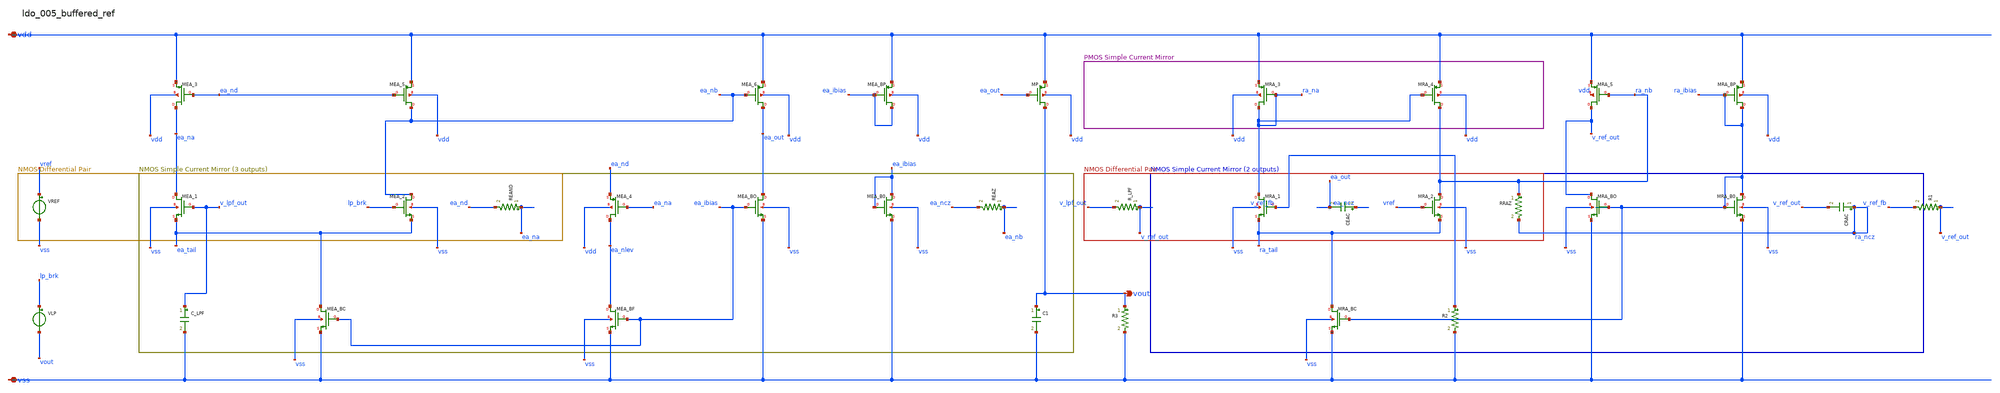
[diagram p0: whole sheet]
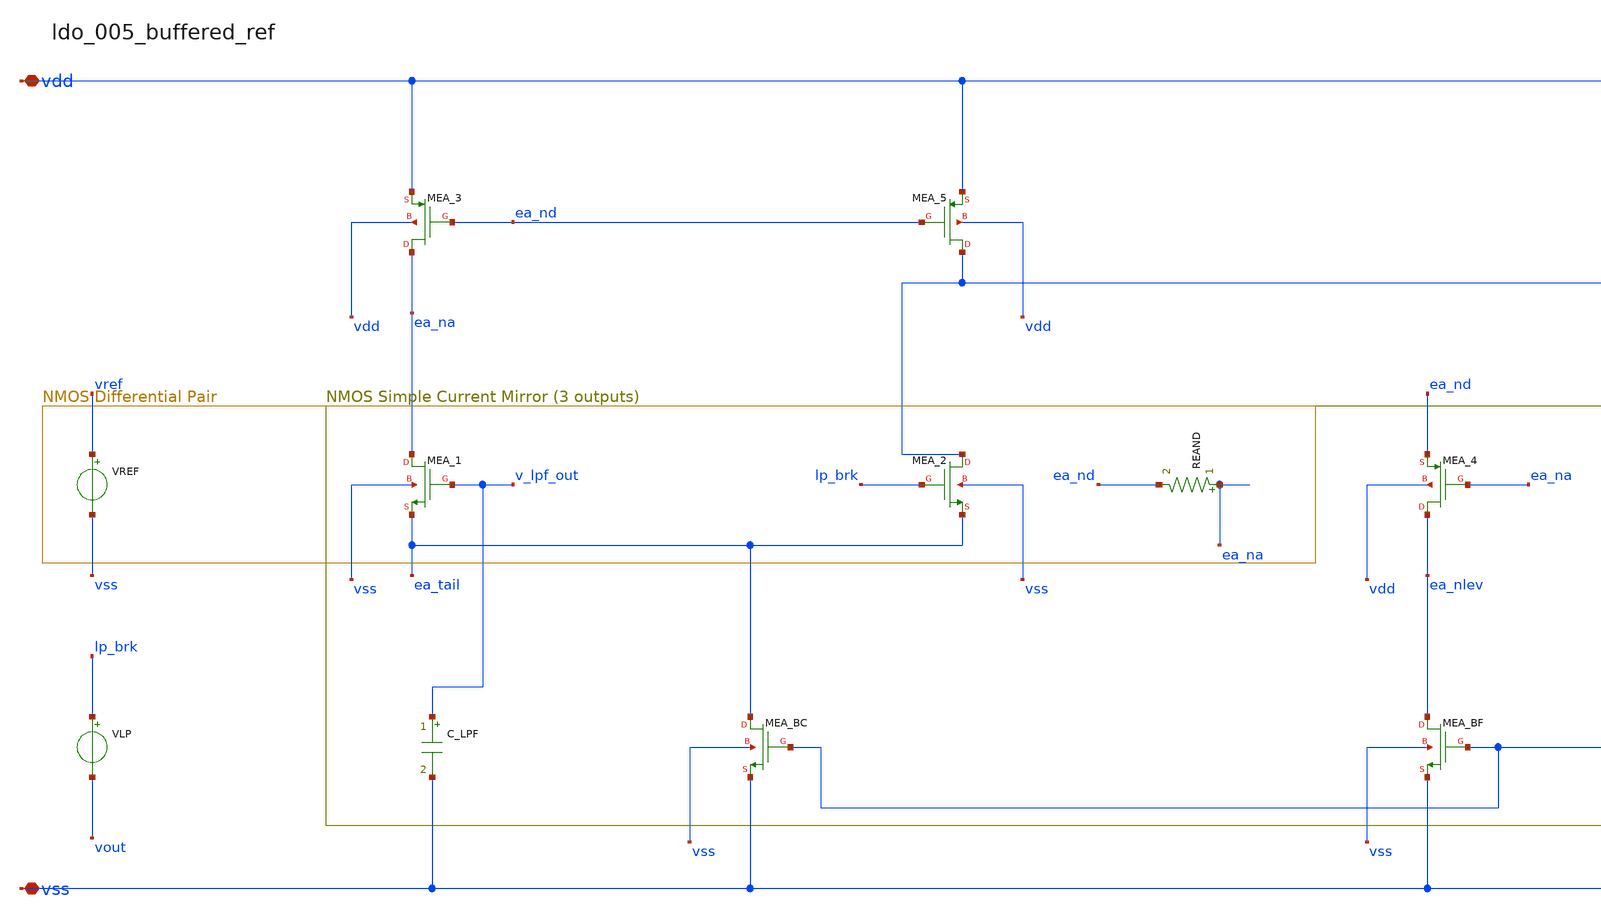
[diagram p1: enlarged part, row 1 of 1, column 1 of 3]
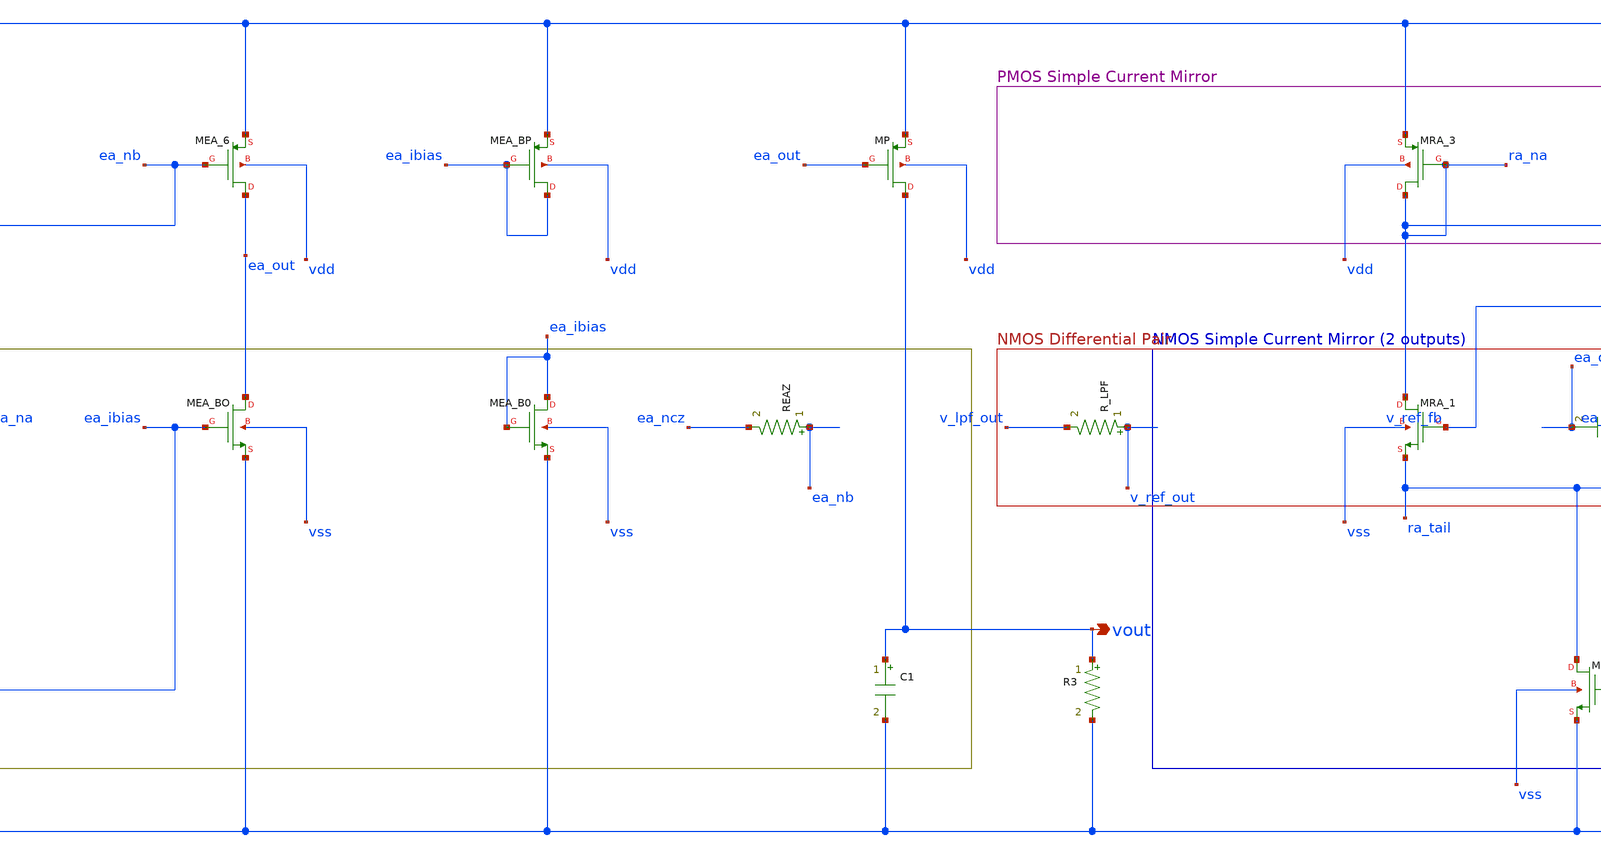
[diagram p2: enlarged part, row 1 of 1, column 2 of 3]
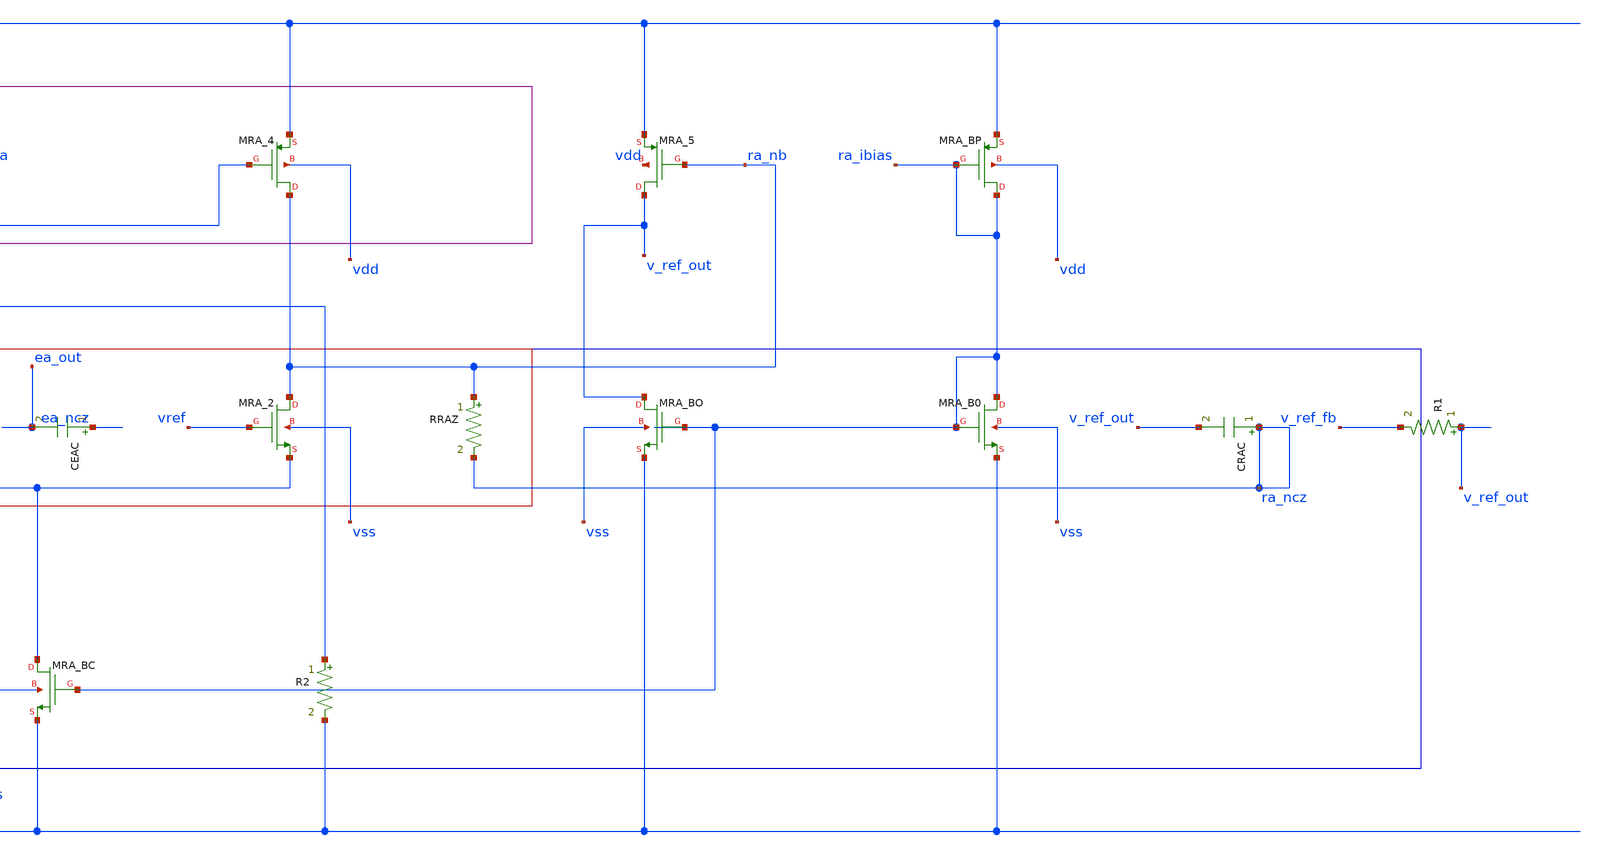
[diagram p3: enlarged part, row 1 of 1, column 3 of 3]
** sch_path: analog-db/raw/ldo_005_buffered_ref/ldo_005_buffered_ref_annotated.sch
**.subckt ldo_005_buffered_ref_annotated vdd vss vout
*.iopin vdd
*.iopin vss
*.opin vout
C1 vout vss 'c_out_int' m=1
CEAC ea_ncz ea_out 'c_ea_comp' m=1
CRAC ra_ncz v_ref_out 'c_ra_comp' m=1
C_LPF v_lpf_out vss 'c_lpf' m=1
R1 v_ref_out v_ref_fb 'r_ref_top' m=1
R2 v_ref_fb vss 'r_ref_bot' m=1
R3 vout vss 'r_bleed' m=1
REAND ea_na ea_nd 'r_ea_nd' m=1
REAZ ea_nb ea_ncz 'r_ea_z' m=1
RRAZ ra_nb ra_ncz 'r_ra_z' m=1
R_LPF v_ref_out v_lpf_out 'r_lpf' m=1
VLP lp_brk vout dc 0
VREF vref vss dc {vref_val}
XMEA_1 ea_na v_lpf_out ea_tail vss sg13_hv_nmos w=x_dut_xmea_1_w l=x_dut_xmea_1_l ng=1 m=1
XMEA_2 ea_nb lp_brk ea_tail vss sg13_hv_nmos w=x_dut_xmea_2_w l=x_dut_xmea_2_l ng=1 m=1
XMEA_3 ea_na ea_nd vdd vdd sg13_hv_pmos w=x_dut_xmea_3_w l=x_dut_xmea_3_l ng=1 m=1
XMEA_4 ea_nlev ea_na ea_nd vdd sg13_hv_pmos w=x_dut_xmea_4_w l=x_dut_xmea_4_l ng=1 m=1
XMEA_5 ea_nb ea_nd vdd vdd sg13_hv_pmos w=x_dut_xmea_5_w l=x_dut_xmea_5_l ng=1 m=1
XMEA_6 ea_out ea_nb vdd vdd sg13_hv_pmos w=x_dut_xmea_6_w l=x_dut_xmea_6_l ng=1 m=1
XMEA_B0 ea_ibias ea_ibias vss vss sg13_hv_nmos w=x_dut_xmea_b0_w l=x_dut_xmea_b0_l ng=1 m=1
XMEA_BC ea_tail ea_ibias vss vss sg13_hv_nmos w=x_dut_xmea_bc_w l=x_dut_xmea_bc_l ng=1 m=1
XMEA_BF ea_nlev ea_ibias vss vss sg13_hv_nmos w=x_dut_xmea_bf_w l=x_dut_xmea_bf_l ng=1 m=1
XMEA_BO ea_out ea_ibias vss vss sg13_hv_nmos w=x_dut_xmea_bo_w l=x_dut_xmea_bo_l ng=1 m=1
XMEA_BP ea_ibias ea_ibias vdd vdd sg13_hv_pmos w=x_dut_xmea_bp_w l=x_dut_xmea_bp_l ng=1 m=1
XMP vout ea_out vdd vdd sg13_hv_pmos w=x_dut_xmp_w l=x_dut_xmp_l ng=1 m=x_dut_xmp_m
XMRA_1 ra_na v_ref_fb ra_tail vss sg13_hv_nmos w=x_dut_xmra_1_w l=x_dut_xmra_1_l ng=1 m=1
XMRA_2 ra_nb vref ra_tail vss sg13_hv_nmos w=x_dut_xmra_2_w l=x_dut_xmra_2_l ng=1 m=1
XMRA_3 ra_na ra_na vdd vdd sg13_hv_pmos w=x_dut_xmra_3_w l=x_dut_xmra_3_l ng=1 m=1
XMRA_4 ra_nb ra_na vdd vdd sg13_hv_pmos w=x_dut_xmra_4_w l=x_dut_xmra_4_l ng=1 m=1
XMRA_5 v_ref_out ra_nb vdd vdd sg13_hv_pmos w=x_dut_xmra_5_w l=x_dut_xmra_5_l ng=1 m=1
XMRA_B0 ra_ibias ra_ibias vss vss sg13_hv_nmos w=x_dut_xmra_b0_w l=x_dut_xmra_b0_l ng=1 m=1
XMRA_BC ra_tail ra_ibias vss vss sg13_hv_nmos w=x_dut_xmra_bc_w l=x_dut_xmra_bc_l ng=1 m=1
XMRA_BO v_ref_out ra_ibias vss vss sg13_hv_nmos w=x_dut_xmra_bo_w l=x_dut_xmra_bo_l ng=1 m=1
XMRA_BP ra_ibias ra_ibias vdd vdd sg13_hv_pmos w=x_dut_xmra_bp_w l=x_dut_xmra_bp_l ng=1 m=1
**.ends
.end
